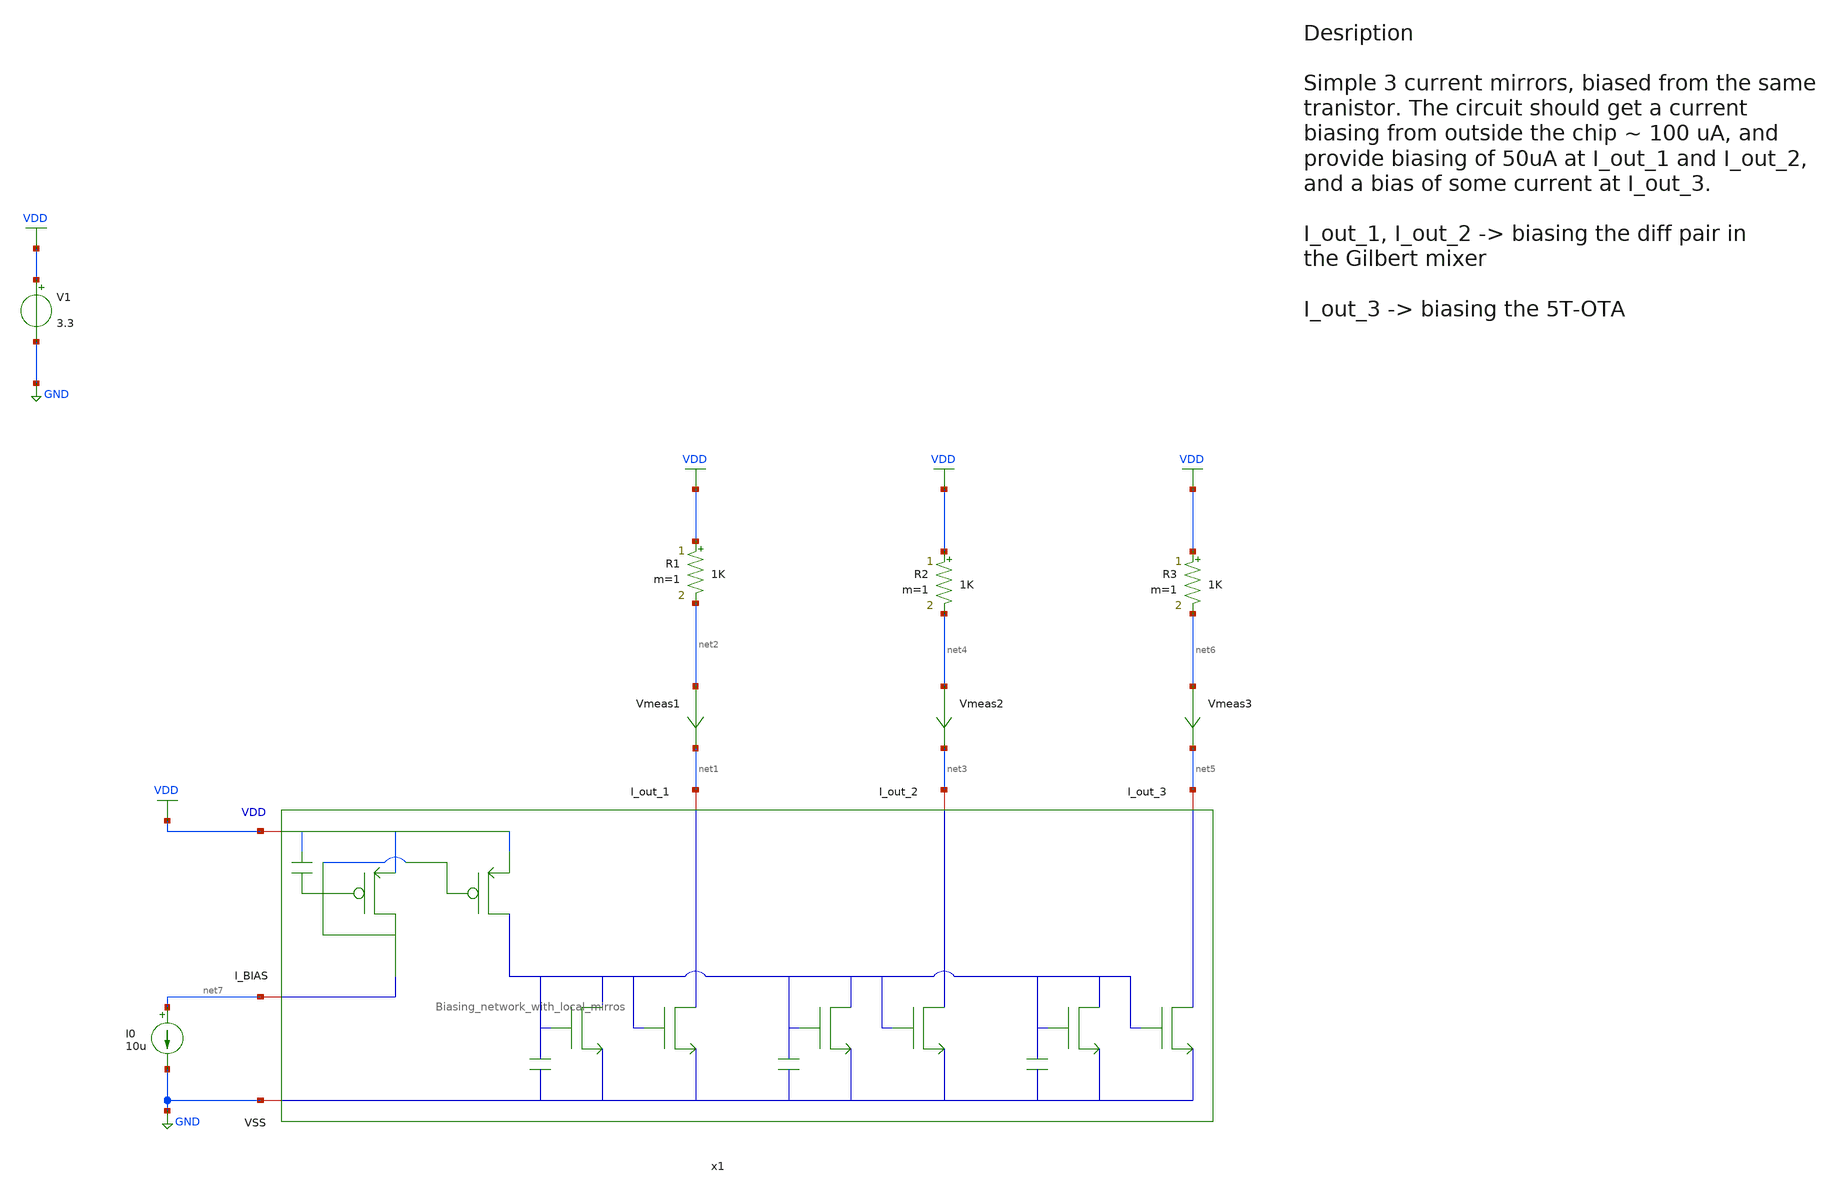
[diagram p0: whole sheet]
** sch_path: src/design_tb/Local_mirror_biasing_tb.sch
**.subckt Local_mirror_biasing_tb
I0 net7 GND 10u
V1 VDD GND 3.3
.save i(v1)
Vmeas1 net2 net1 0
.save i(vmeas1)
Vmeas2 net4 net3 0
.save i(vmeas2)
Vmeas3 net6 net5 0
.save i(vmeas3)
R1 VDD net2 1K m=1
R2 VDD net4 1K m=1
R3 VDD net6 1K m=1
x1 VDD net1 net3 net5 net7 GND Biasing_network_with_local_mirros
**** begin user architecture code

.include $::180MCU_MODELS/design.ngspice
.lib $::180MCU_MODELS/sm141064.ngspice typical
.lib $::180MCU_MODELS/sm141064.ngspice mimcap_typical
.lib $::180MCU_MODELS/sm141064.ngspice cap_mim
.lib $::180MCU_MODELS/sm141064.ngspice res_typical
.lib $::180MCU_MODELS/sm141064.ngspice diode_typical
.lib $::180MCU_MODELS/sm141064.ngspice bjt_typical
.lib $::180MCU_MODELS/sm141064.ngspice moscap_typical
.lib $::180MCU_MODELS/sm141064.ngspice mimcap_typical



* Add convergence aids
.option method=gear

.control

    * operating point
    op
    show

    write Local_mirror_biasing_tb.raw

    set appendwrite

    * Transient analysis to observe mixing operation
    tran 1n 0.01u
    write Local_mirror_biasing_tb.raw

.endc


**** end user architecture code
**.ends
.GLOBAL GND
.GLOBAL VDD
.end
